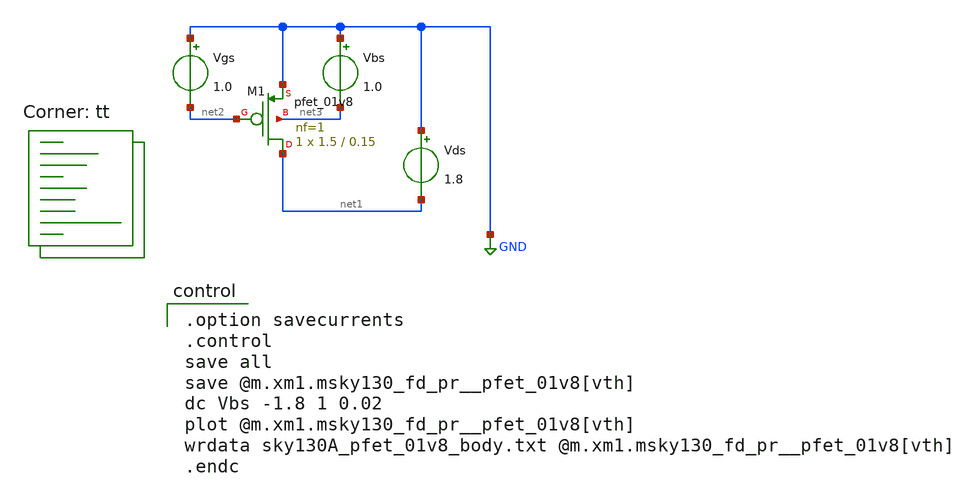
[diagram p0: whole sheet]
** sch_path: xschem/MOSFET/sky130A_pfet_01v8_body.sch
**.subckt sky130A_pfet_01v8_body
Vgs GND net2 1.0
Vds GND net1 1.8
Vbs GND net3 1.0
XM1 net1 net2 GND net3 sky130_fd_pr__pfet_01v8 L=0.15 W=1.5 nf=1 ad='int((nf+1)/2) * W/nf * 0.29' as='int((nf+2)/2) * W/nf * 0.29'
+ pd='2*int((nf+1)/2) * (W/nf + 0.29)' ps='2*int((nf+2)/2) * (W/nf + 0.29)' nrd='0.29 / W' nrs='0.29 / W'
+ sa=0 sb=0 sd=0 mult=1 m=1
**** begin user architecture code

.option savecurrents
.control
save all
save @m.xm1.msky130_fd_pr__pfet_01v8[vth]
dc Vbs -1.8 1 0.02
plot @m.xm1.msky130_fd_pr__pfet_01v8[vth]
wrdata sky130A_pfet_01v8_body.txt @m.xm1.msky130_fd_pr__pfet_01v8[vth]
.endc

.lib $::SKYWATER_MODELS/sky130.lib.spice tt
**** end user architecture code
**.ends
.GLOBAL GND
.end
